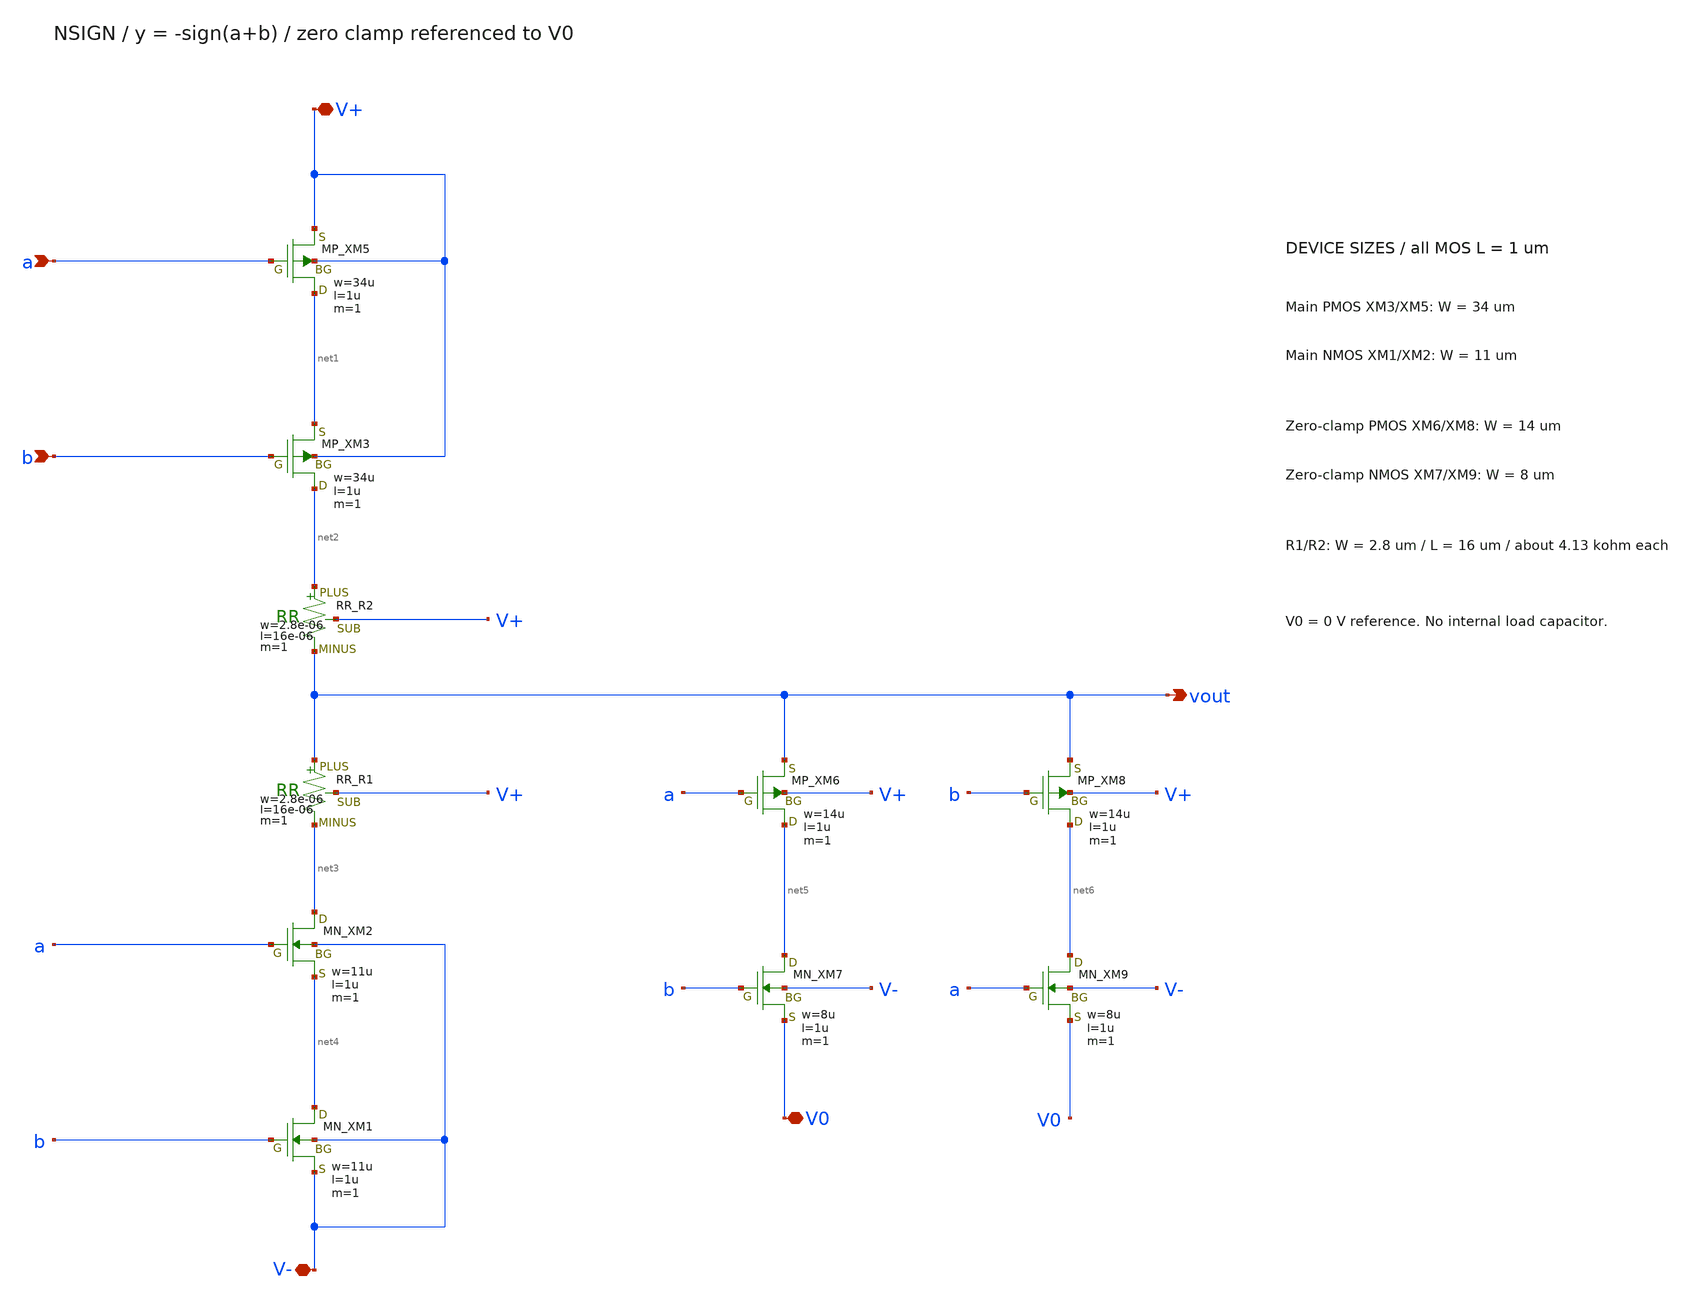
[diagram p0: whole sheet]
** sch_path: member_project/balanced-ternary-logic/PenguinEino/nsign.sch
**.subckt nsign V+ a b vout V- V0
*.iopin V+
*.ipin a
*.ipin b
*.opin vout
*.iopin V-
*.iopin V0
XXM3 net2 b net1 V+ PMOS w=34u l=1u nrd=0 nrs=0 m=1
XR2 net2 vout V+ F_RR w=2.8e-06 l=16e-06 R=1 tc1=0 tc2=0 m=1
XR1 vout net3 V+ F_RR w=2.8e-06 l=16e-06 R=1 tc1=0 tc2=0 m=1
XXM2 net3 a net4 V- NMOS w=11u l=1u nrd=0 nrs=0 m=1
XXM1 net4 b V- V- NMOS w=11u l=1u nrd=0 nrs=0 m=1
XXM5 net1 a V+ V+ PMOS w=34u l=1u nrd=0 nrs=0 m=1
XXM6 net5 a vout V+ PMOS w=14u l=1u nrd=0 nrs=0 m=1
XXM7 net5 b V0 V- NMOS w=8u l=1u nrd=0 nrs=0 m=1
XXM8 net6 b vout V+ PMOS w=14u l=1u nrd=0 nrs=0 m=1
XXM9 net6 a V0 V- NMOS w=8u l=1u nrd=0 nrs=0 m=1
**.ends
.end
